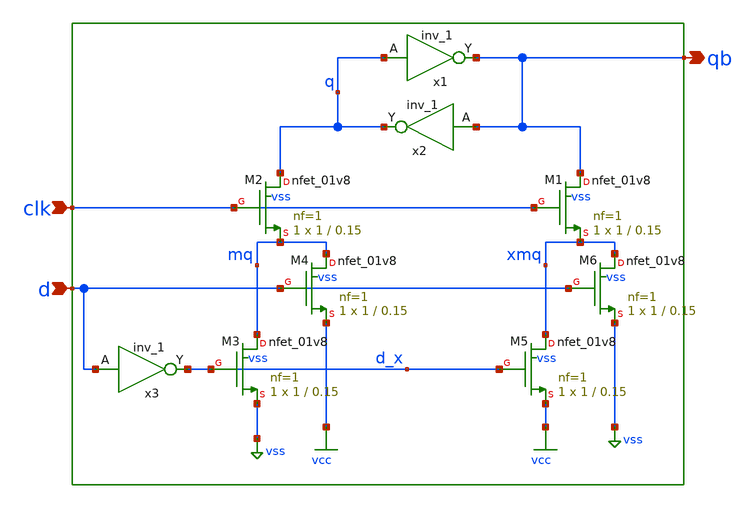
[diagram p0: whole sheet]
** sch_path: src/xe/test_cases/cascode_latch.sch
**.subckt cascode_latch d clk qb
*.ipin d
*.ipin clk
*.opin qb
x1 q vss vss vcc vcc qb sky130_fd_sc_hd__inv_1
x2 qb vss vss vcc vcc q sky130_fd_sc_hd__inv_1
XM1 qb clk xmq vss sky130_fd_pr__nfet_01v8 L=0.15 W=1 nf=1 ad='int((nf+1)/2) * W/nf * 0.29' as='int((nf+2)/2) * W/nf * 0.29'
+ pd='2*int((nf+1)/2) * (W/nf + 0.29)' ps='2*int((nf+2)/2) * (W/nf + 0.29)' nrd='0.29 / W' nrs='0.29 / W'
+ sa=0 sb=0 sd=0 mult=1 m=1
XM2 q clk mq vss sky130_fd_pr__nfet_01v8 L=0.15 W=1 nf=1 ad='int((nf+1)/2) * W/nf * 0.29' as='int((nf+2)/2) * W/nf * 0.29'
+ pd='2*int((nf+1)/2) * (W/nf + 0.29)' ps='2*int((nf+2)/2) * (W/nf + 0.29)' nrd='0.29 / W' nrs='0.29 / W'
+ sa=0 sb=0 sd=0 mult=1 m=1
XM3 mq d_x vss vss sky130_fd_pr__nfet_01v8 L=0.15 W=1 nf=1 ad='int((nf+1)/2) * W/nf * 0.29' as='int((nf+2)/2) * W/nf * 0.29'
+ pd='2*int((nf+1)/2) * (W/nf + 0.29)' ps='2*int((nf+2)/2) * (W/nf + 0.29)' nrd='0.29 / W' nrs='0.29 / W'
+ sa=0 sb=0 sd=0 mult=1 m=1
XM4 mq d vcc vss sky130_fd_pr__nfet_01v8 L=0.15 W=1 nf=1 ad='int((nf+1)/2) * W/nf * 0.29' as='int((nf+2)/2) * W/nf * 0.29'
+ pd='2*int((nf+1)/2) * (W/nf + 0.29)' ps='2*int((nf+2)/2) * (W/nf + 0.29)' nrd='0.29 / W' nrs='0.29 / W'
+ sa=0 sb=0 sd=0 mult=1 m=1
XM5 xmq d_x vcc vss sky130_fd_pr__nfet_01v8 L=0.15 W=1 nf=1 ad='int((nf+1)/2) * W/nf * 0.29' as='int((nf+2)/2) * W/nf * 0.29'
+ pd='2*int((nf+1)/2) * (W/nf + 0.29)' ps='2*int((nf+2)/2) * (W/nf + 0.29)' nrd='0.29 / W' nrs='0.29 / W'
+ sa=0 sb=0 sd=0 mult=1 m=1
XM6 xmq d vss vss sky130_fd_pr__nfet_01v8 L=0.15 W=1 nf=1 ad='int((nf+1)/2) * W/nf * 0.29' as='int((nf+2)/2) * W/nf * 0.29'
+ pd='2*int((nf+1)/2) * (W/nf + 0.29)' ps='2*int((nf+2)/2) * (W/nf + 0.29)' nrd='0.29 / W' nrs='0.29 / W'
+ sa=0 sb=0 sd=0 mult=1 m=1
x3 d vss vss vcc vcc d_x sky130_fd_sc_hd__inv_1
**.ends
.GLOBAL vcc
.GLOBAL vss
.end
